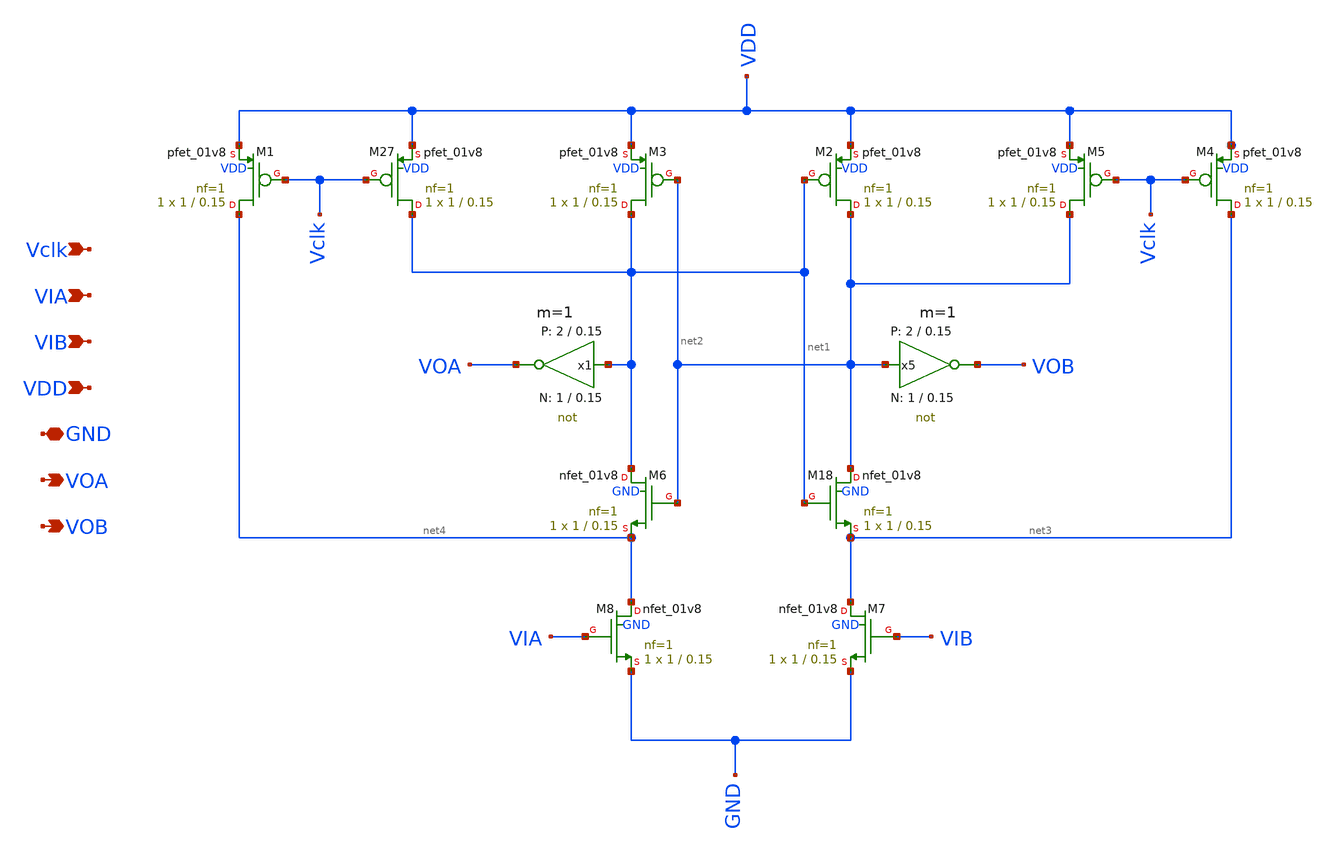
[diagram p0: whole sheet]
** sch_path: Comparator.sch
* StefanSchippers/xschem_sky130/sky130_tests/not.sch:
* Copyright 2021 Stefan Frederik Schippers
* Licensed under the Apache License, Version 2.0 (the "License");
**.subckt Comparator Vclk VIA VIB VDD GND VOA VOB
*.ipin Vclk
*.ipin VIA
*.ipin VIB
*.ipin VDD
*.iopin GND
*.opin VOA
*.opin VOB
XM27 net1 Vclk VDD VDD sky130_fd_pr__pfet_01v8 L=0.15 W=1 nf=1 ad='int((1 + 1)/2) * 1 / 1 * 0.29' as='int((1 + 2)/2) * 1 / 1 * 0.29'
+ pd='2*int((1 + 1)/2) * (1 / 1 + 0.29)' ps='2*int((1 + 2)/2) * (1 / 1 + 0.29)' nrd='0.29 / 1 ' nrs='0.29 / 1 '
+ sa=0 sb=0 sd=0 mult=1 m=1
XM1 net4 Vclk VDD VDD sky130_fd_pr__pfet_01v8 L=0.15 W=1 nf=1 ad='int((1 + 1)/2) * 1 / 1 * 0.29' as='int((1 + 2)/2) * 1 / 1 * 0.29'
+ pd='2*int((1 + 1)/2) * (1 / 1 + 0.29)' ps='2*int((1 + 2)/2) * (1 / 1 + 0.29)' nrd='0.29 / 1 ' nrs='0.29 / 1 '
+ sa=0 sb=0 sd=0 mult=1 m=1
XM2 net2 net1 VDD VDD sky130_fd_pr__pfet_01v8 L=0.15 W=1 nf=1 ad='int((1 + 1)/2) * 1 / 1 * 0.29' as='int((1 + 2)/2) * 1 / 1 * 0.29'
+ pd='2*int((1 + 1)/2) * (1 / 1 + 0.29)' ps='2*int((1 + 2)/2) * (1 / 1 + 0.29)' nrd='0.29 / 1 ' nrs='0.29 / 1 '
+ sa=0 sb=0 sd=0 mult=1 m=1
XM3 net1 net2 VDD VDD sky130_fd_pr__pfet_01v8 L=0.15 W=1 nf=1 ad='int((1 + 1)/2) * 1 / 1 * 0.29' as='int((1 + 2)/2) * 1 / 1 * 0.29'
+ pd='2*int((1 + 1)/2) * (1 / 1 + 0.29)' ps='2*int((1 + 2)/2) * (1 / 1 + 0.29)' nrd='0.29 / 1 ' nrs='0.29 / 1 '
+ sa=0 sb=0 sd=0 mult=1 m=1
XM4 net3 Vclk VDD VDD sky130_fd_pr__pfet_01v8 L=0.15 W=1 nf=1 ad='int((1 + 1)/2) * 1 / 1 * 0.29' as='int((1 + 2)/2) * 1 / 1 * 0.29'
+ pd='2*int((1 + 1)/2) * (1 / 1 + 0.29)' ps='2*int((1 + 2)/2) * (1 / 1 + 0.29)' nrd='0.29 / 1 ' nrs='0.29 / 1 '
+ sa=0 sb=0 sd=0 mult=1 m=1
XM5 net2 Vclk VDD VDD sky130_fd_pr__pfet_01v8 L=0.15 W=1 nf=1 ad='int((1 + 1)/2) * 1 / 1 * 0.29' as='int((1 + 2)/2) * 1 / 1 * 0.29'
+ pd='2*int((1 + 1)/2) * (1 / 1 + 0.29)' ps='2*int((1 + 2)/2) * (1 / 1 + 0.29)' nrd='0.29 / 1 ' nrs='0.29 / 1 '
+ sa=0 sb=0 sd=0 mult=1 m=1
x5 VOB net2 VCC VSS not W_N=1 L_N=0.15 W_P=2 L_P=0.15 m=1
x1 VOA net1 VCC VSS not W_N=1 L_N=0.15 W_P=2 L_P=0.15 m=1
XM18 net2 net1 net3 GND sky130_fd_pr__nfet_01v8 L=0.15 W=1 nf=1 ad='int((nf+1)/2) * W/nf * 0.29' as='int((nf+2)/2) * W/nf * 0.29'
+ pd='2*int((nf+1)/2) * (W/nf + 0.29)' ps='2*int((nf+2)/2) * (W/nf + 0.29)' nrd='0.29 / W' nrs='0.29 / W'
+ sa=0 sb=0 sd=0 mult=1 m=1
XM6 net1 net2 net4 GND sky130_fd_pr__nfet_01v8 L=0.15 W=1 nf=1 ad='int((nf+1)/2) * W/nf * 0.29' as='int((nf+2)/2) * W/nf * 0.29'
+ pd='2*int((nf+1)/2) * (W/nf + 0.29)' ps='2*int((nf+2)/2) * (W/nf + 0.29)' nrd='0.29 / W' nrs='0.29 / W'
+ sa=0 sb=0 sd=0 mult=1 m=1
XM7 net3 VIB GND GND sky130_fd_pr__nfet_01v8 L=0.15 W=1 nf=1 ad='int((nf+1)/2) * W/nf * 0.29' as='int((nf+2)/2) * W/nf * 0.29'
+ pd='2*int((nf+1)/2) * (W/nf + 0.29)' ps='2*int((nf+2)/2) * (W/nf + 0.29)' nrd='0.29 / W' nrs='0.29 / W'
+ sa=0 sb=0 sd=0 mult=1 m=1
XM8 net4 VIA GND GND sky130_fd_pr__nfet_01v8 L=0.15 W=1 nf=1 ad='int((nf+1)/2) * W/nf * 0.29' as='int((nf+2)/2) * W/nf * 0.29'
+ pd='2*int((nf+1)/2) * (W/nf + 0.29)' ps='2*int((nf+2)/2) * (W/nf + 0.29)' nrd='0.29 / W' nrs='0.29 / W'
+ sa=0 sb=0 sd=0 mult=1 m=1
**.ends

* expanding   symbol:  sky130_tests/not.sym # of pins=2
** sym_path: sky130_tests/not.sym
** sch_path: sky130_tests/not.sch
.subckt not y a VCCPIN VSSPIN     W_N=1 L_N=0.15 W_P=2 L_P=0.15
*.opin y
*.ipin a
XM1 DN a VSSPIN VSSPIN sky130_fd_pr__nfet_01v8 L=L_N W=W_N nf=1 ad='int((1 + 1)/2) * W_N / 1 * 0.29'
+ as='int((1 + 2)/2) * W_N / 1 * 0.29' pd='2*int((1 + 1)/2) * (W_N / 1 + 0.29)' ps='2*int((1 + 2)/2) * (W_N / 1 + 0.29)'
+ nrd='0.29 / W_N ' nrs='0.29 / W_N ' sa=0 sb=0 sd=0 mult=1 m=1
XM2 DP a VCCPIN VCCPIN sky130_fd_pr__pfet_01v8 L=L_P W=W_P nf=1 ad='int((nf+1)/2) * W/nf * 0.29' as='int((nf+2)/2) * W/nf * 0.29'
+ pd='2*int((nf+1)/2) * (W/nf + 0.29)' ps='2*int((nf+2)/2) * (W/nf + 0.29)' nrd='0.29 / W' nrs='0.29 / W'
+ sa=0 sb=0 sd=0 mult=1 m=1
Vmeas DP y 0
.save i(vmeas)
Vmeas1 y DN 0
.save i(vmeas1)
.save v(dp)
.save v(dn)
.ends

.end
